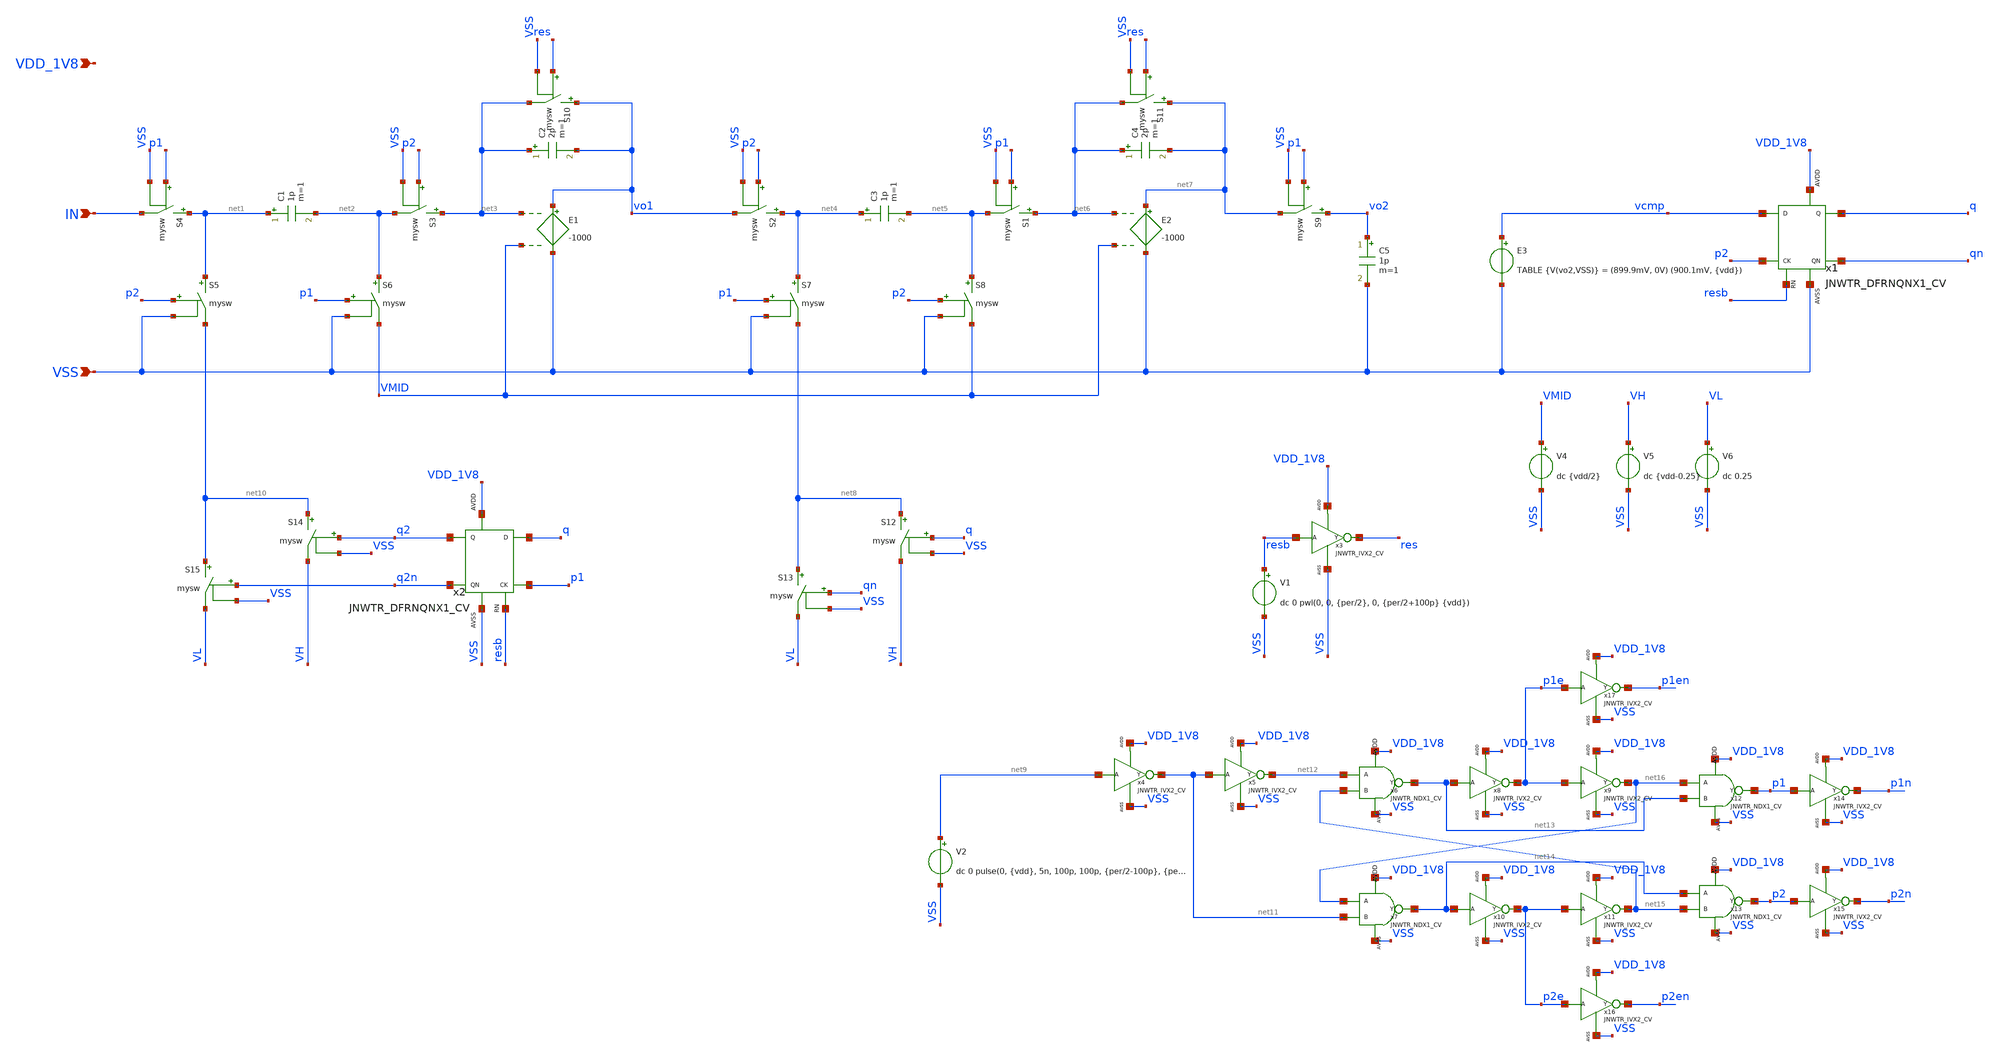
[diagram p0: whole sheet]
** sch_path: design/JNW_SIGMA_DELTA_A2D_SKY130A/JNW_SIGMA_DELTA_A2D.sch
**.subckt JNW_SIGMA_DELTA_A2D VDD_1V8 VSS IN
*.ipin VDD_1V8
*.ipin VSS
*.ipin IN
C1 net1 net2 1p m=1
E1 vo1 VSS net3 VMID -1000
C2 net3 vo1 2p m=1
C3 net4 net5 1p m=1
E2 net7 VSS net6 VMID -1000
C4 net6 net7 2p m=1
S9 vo2 net7 p1 VSS mysw
C5 vo2 VSS 1p m=1
S1 net6 net5 p1 VSS mysw
S2 net4 vo1 p2 VSS mysw
S3 net3 net2 p2 VSS mysw
S4 net1 IN p1 VSS mysw
S5 net1 net10 p2 VSS mysw
S6 net2 VMID p1 VSS mysw
S7 net4 net8 p1 VSS mysw
S8 net5 VMID p2 VSS mysw
E3 vcmp VSS TABLE {V(vo2,VSS)} = (899.9mV, 0V) (900.1mV, {vdd})
x1 vcmp p2 resb q qn VDD_1V8 VSS JNWTR_DFRNQNX1_CV xoffset=0 yoffset=0 angle=0
x2 q p1 resb q2 q2n VDD_1V8 VSS JNWTR_DFRNQNX1_CV xoffset=0 yoffset=0 angle=0
V1 resb VSS dc 0 pwl(0, 0, {per/2}, 0, {per/2+100p} {vdd})
V2 net9 VSS dc 0 pulse(0, {vdd}, 5n, 100p, 100p, {per/2-100p}, {per})
S10 vo1 net3 res VSS mysw
S11 net7 net6 res VSS mysw
x3 resb res VDD_1V8 VSS JNWTR_IVX2_CV xoffset=0 yoffset=0 angle=0 M=1
S12 net8 VH q VSS mysw
S13 net8 VL qn VSS mysw
S14 net10 VH q2 VSS mysw
S15 net10 VL q2n VSS mysw
V4 VMID VSS dc {vdd/2}
V5 VH VSS dc {vdd-0.25}
V6 VL VSS dc 0.25
x4 net9 net11 VDD_1V8 VSS JNWTR_IVX2_CV xoffset=0 yoffset=0 angle=0 M=1
x5 net11 net12 VDD_1V8 VSS JNWTR_IVX2_CV xoffset=0 yoffset=0 angle=0 M=1
x6 net12 net15 net13 VDD_1V8 VSS JNWTR_NDX1_CV
x7 net16 net11 net14 VDD_1V8 VSS JNWTR_NDX1_CV
x8 net13 p1e VDD_1V8 VSS JNWTR_IVX2_CV xoffset=0 yoffset=0 angle=0 M=1
x9 p1e net16 VDD_1V8 VSS JNWTR_IVX2_CV xoffset=0 yoffset=0 angle=0 M=1
x10 net14 p2e VDD_1V8 VSS JNWTR_IVX2_CV xoffset=0 yoffset=0 angle=0 M=1
x11 p2e net15 VDD_1V8 VSS JNWTR_IVX2_CV xoffset=0 yoffset=0 angle=0 M=1
x12 net16 net13 p1 VDD_1V8 VSS JNWTR_NDX1_CV
x13 net14 net15 p2 VDD_1V8 VSS JNWTR_NDX1_CV
x14 p1 p1n VDD_1V8 VSS JNWTR_IVX2_CV xoffset=0 yoffset=0 angle=0 M=1
x15 p2 p2n VDD_1V8 VSS JNWTR_IVX2_CV xoffset=0 yoffset=0 angle=0 M=1
x16 p2e p2en VDD_1V8 VSS JNWTR_IVX2_CV xoffset=0 yoffset=0 angle=0 M=1
x17 p1e p1en VDD_1V8 VSS JNWTR_IVX2_CV xoffset=0 yoffset=0 angle=0 M=1
**.ends
.end
